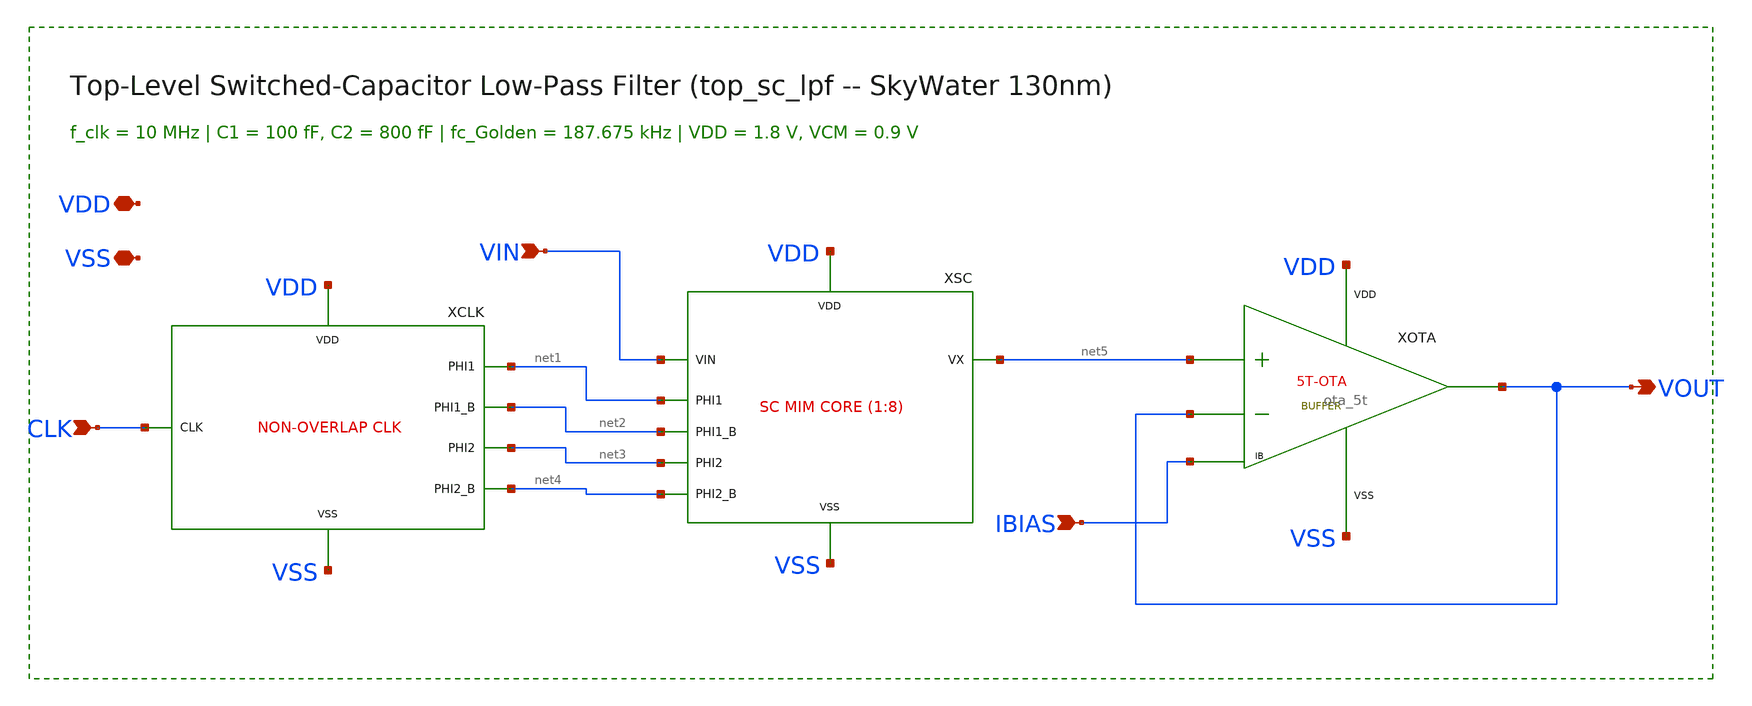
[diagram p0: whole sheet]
** sch_path: sky130-sc-lpf/xschem/top_sc_lpf.sch
**.subckt top_sc_lpf VDD VSS CLK VIN IBIAS VOUT
*.iopin VDD
*.iopin VSS
*.ipin CLK
*.ipin VIN
*.ipin IBIAS
*.opin VOUT
XCLK CLK net1 net2 net3 net4 VDD VSS non_overlap_clk
XSC VIN net5 net1 net2 net3 net4 VDD VSS sc_core
XOTA net5 VOUT IBIAS VOUT VDD VSS ota_5t
**.ends

* expanding   symbol:  non_overlap_clk.sym # of pins=7
** sym_path: sky130-sc-lpf/xschem/non_overlap_clk.sym
** sch_path: sky130-sc-lpf/xschem/non_overlap_clk.sch
.subckt non_overlap_clk CLK PHI1 PHI1_B PHI2 PHI2_B VDD VSS
*.iopin VDD
*.iopin VSS
*.ipin CLK
*.opin PHI1
*.opin PHI1_B
*.opin PHI2
*.opin PHI2_B
XINV0 CLK net1 VDD VSS inv_cell WN=1.0 WP=2.5 LCH=0.15
XNAND_A CLK net15 net2 VDD VSS nand2_cell
XNAND_B net14 net1 net3 VDD VSS nand2_cell
XDA1 net2 net4 VDD VSS inv_cell WN=0.6 WP=1.5 LCH=0.95
XDB1 net3 net5 VDD VSS inv_cell WN=0.6 WP=1.5 LCH=0.95
XDA2 net4 net6 VDD VSS inv_cell WN=0.6 WP=1.5 LCH=0.95
XDB2 net5 net7 VDD VSS inv_cell WN=0.6 WP=1.5 LCH=0.95
XDA3 net6 net8 VDD VSS inv_cell WN=0.6 WP=1.5 LCH=0.95
XDB3 net7 net9 VDD VSS inv_cell WN=0.6 WP=1.5 LCH=0.95
XDA4 net8 net10 VDD VSS inv_cell WN=0.6 WP=1.5 LCH=0.95
XDB4 net9 net11 VDD VSS inv_cell WN=0.6 WP=1.5 LCH=0.95
XDA5 net10 net12 VDD VSS inv_cell WN=0.6 WP=1.5 LCH=0.95
XDB5 net11 net13 VDD VSS inv_cell WN=0.6 WP=1.5 LCH=0.95
XDA6 net12 net14 VDD VSS inv_cell WN=0.6 WP=1.5 LCH=0.95
XDB6 net13 net15 VDD VSS inv_cell WN=0.6 WP=1.5 LCH=0.95
XBUF1A net14 PHI1 VDD VSS inv_cell WN=2.0 WP=6.0 LCH=0.15
XBUF1B PHI1 PHI1_B VDD VSS inv_cell WN=2.0 WP=6.0 LCH=0.15
XBUF2A net15 PHI2 VDD VSS inv_cell WN=2.0 WP=6.0 LCH=0.15
XBUF2B PHI2 PHI2_B VDD VSS inv_cell WN=2.0 WP=6.0 LCH=0.15
.ends


* expanding   symbol:  sc_core.sym # of pins=8
** sym_path: sky130-sc-lpf/xschem/sc_core.sym
** sch_path: sky130-sc-lpf/xschem/sc_core.sch
.subckt sc_core VIN VX PHI1 PHI1_B PHI2 PHI2_B VDD VSS
*.iopin VDD
*.iopin VSS
*.ipin PHI1
*.ipin PHI1_B
*.ipin PHI2
*.ipin PHI2_B
*.ipin VIN
*.opin VX
XTG1 VIN net1 PHI1 PHI1_B VDD VSS tg_switch
XC1 net1 VSS sky130_fd_pr__cap_mim_m3_1 W=4.85 L=9.85 MF=1 m=1
XTG2 net1 VX PHI2 PHI2_B VDD VSS tg_switch
XC2 VX VSS sky130_fd_pr__cap_mim_m3_1 W=4.85 L=9.85 MF=8 m=8
XDUM2 VX PHI2_B PHI2 VDD VSS tg_dummy
.ends


* expanding   symbol:  ota_5t.sym # of pins=6
** sym_path: sky130-sc-lpf/xschem/ota_5t.sym
** sch_path: sky130-sc-lpf/xschem/ota_5t.sch
.subckt ota_5t INP INN IBIAS VOUT VDD VSS
*.iopin VDD
*.opin VOUT
*.ipin INP
*.ipin INN
*.ipin IBIAS
*.iopin VSS
XM3 net1 net1 VDD VDD sky130_fd_pr__pfet_01v8 L=0.80 W=16.0 nf=4 ad='int((nf+1)/2) * W/nf * 0.29' as='int((nf+2)/2) * W/nf * 0.29'
+ pd='2*int((nf+1)/2) * (W/nf + 0.29)' ps='2*int((nf+2)/2) * (W/nf + 0.29)' nrd='0.29 / W' nrs='0.29 / W'
+ sa=0 sb=0 sd=0 mult=1 m=1
XM4 VOUT net1 VDD VDD sky130_fd_pr__pfet_01v8 L=0.80 W=16.0 nf=4 ad='int((nf+1)/2) * W/nf * 0.29' as='int((nf+2)/2) * W/nf * 0.29'
+ pd='2*int((nf+1)/2) * (W/nf + 0.29)' ps='2*int((nf+2)/2) * (W/nf + 0.29)' nrd='0.29 / W' nrs='0.29 / W'
+ sa=0 sb=0 sd=0 mult=1 m=1
XM1 net1 INP net2 VSS sky130_fd_pr__nfet_01v8 L=0.80 W=32.0 nf=8 ad='int((8 + 1)/2) * 32.0 / 8 * 0.29'
+ as='int((8 + 2)/2) * 32.0 / 8 * 0.29' pd='2*int((8 + 1)/2) * (32.0 / 8 + 0.29)' ps='2*int((8 + 2)/2) * (32.0 / 8 + 0.29)'
+ nrd='0.29 / 32.0 ' nrs='0.29 / 32.0 ' sa=0 sb=0 sd=0 mult=1 m=1
XM2 VOUT INN net2 VSS sky130_fd_pr__nfet_01v8 L=0.80 W=32.0 nf=8 ad='int((8 + 1)/2) * 32.0 / 8 * 0.29'
+ as='int((8 + 2)/2) * 32.0 / 8 * 0.29' pd='2*int((8 + 1)/2) * (32.0 / 8 + 0.29)' ps='2*int((8 + 2)/2) * (32.0 / 8 + 0.29)'
+ nrd='0.29 / 32.0 ' nrs='0.29 / 32.0 ' sa=0 sb=0 sd=0 mult=1 m=1
XM5 net2 IBIAS VSS VSS sky130_fd_pr__nfet_01v8 L=1.00 W=24.0 nf=6 ad='int((6 + 1)/2) * 24.0 / 6 * 0.29'
+ as='int((6 + 2)/2) * 24.0 / 6 * 0.29' pd='2*int((6 + 1)/2) * (24.0 / 6 + 0.29)' ps='2*int((6 + 2)/2) * (24.0 / 6 + 0.29)'
+ nrd='0.29 / 24.0 ' nrs='0.29 / 24.0 ' sa=0 sb=0 sd=0 mult=1 m=1
XM6 IBIAS IBIAS VSS VSS sky130_fd_pr__nfet_01v8 L=1.00 W=24.0 nf=6 ad='int((6 + 1)/2) * 24.0 / 6 * 0.29'
+ as='int((6 + 2)/2) * 24.0 / 6 * 0.29' pd='2*int((6 + 1)/2) * (24.0 / 6 + 0.29)' ps='2*int((6 + 2)/2) * (24.0 / 6 + 0.29)'
+ nrd='0.29 / 24.0 ' nrs='0.29 / 24.0 ' sa=0 sb=0 sd=0 mult=1 m=1
.ends


* expanding   symbol:  inv_cell.sym # of pins=4
** sym_path: sky130-sc-lpf/xschem/inv_cell.sym
** sch_path: sky130-sc-lpf/xschem/inv_cell.sch
.subckt inv_cell A Y VDD VSS  WN=1.0 WP=2.5 LCH=0.15
*.ipin A
*.opin Y
*.iopin VDD
*.iopin VSS
XMP Y A VDD VDD sky130_fd_pr__pfet_01v8 L='LCH' W='WP' nf=1 ad='WP*0.29' as='WP*0.29' pd='2*(WP+0.29)'
+ ps='2*(WP+0.29)' nrd='0.29/WP' nrs='0.29/WP' sa=0 sb=0 sd=0 mult=1 m=1
XMN Y A VSS VSS sky130_fd_pr__nfet_01v8 L='LCH' W='WN' nf=1 ad='WN*0.29' as='WN*0.29' pd='2*(WN+0.29)'
+ ps='2*(WN+0.29)' nrd='0.29/WN' nrs='0.29/WN' sa=0 sb=0 sd=0 mult=1 m=1
.ends


* expanding   symbol:  nand2_cell.sym # of pins=5
** sym_path: sky130-sc-lpf/xschem/nand2_cell.sym
** sch_path: sky130-sc-lpf/xschem/nand2_cell.sch
.subckt nand2_cell A B Y VDD VSS
*.iopin VDD
*.opin Y
*.iopin VSS
*.ipin A
*.ipin B
XMPA Y A VDD VDD sky130_fd_pr__pfet_01v8 L=0.15 W=2.0 nf=1 ad='int((nf+1)/2) * W/nf * 0.29' as='int((nf+2)/2) * W/nf * 0.29'
+ pd='2*int((nf+1)/2) * (W/nf + 0.29)' ps='2*int((nf+2)/2) * (W/nf + 0.29)' nrd='0.29 / W' nrs='0.29 / W'
+ sa=0 sb=0 sd=0 mult=1 m=1
XMPB Y B VDD VDD sky130_fd_pr__pfet_01v8 L=0.15 W=2.0 nf=1 ad='int((nf+1)/2) * W/nf * 0.29' as='int((nf+2)/2) * W/nf * 0.29'
+ pd='2*int((nf+1)/2) * (W/nf + 0.29)' ps='2*int((nf+2)/2) * (W/nf + 0.29)' nrd='0.29 / W' nrs='0.29 / W'
+ sa=0 sb=0 sd=0 mult=1 m=1
XMNA Y A net1 VSS sky130_fd_pr__nfet_01v8 L=0.15 W=1.6 nf=1 ad='int((1 + 1)/2) * 1.6 / 1 * 0.29' as='int((1 + 2)/2) * 1.6 / 1 * 0.29'
+ pd='2*int((1 + 1)/2) * (1.6 / 1 + 0.29)' ps='2*int((1 + 2)/2) * (1.6 / 1 + 0.29)' nrd='0.29 / 1.6 ' nrs='0.29 / 1.6 '
+ sa=0 sb=0 sd=0 mult=1 m=1
XMNB net1 B VSS VSS sky130_fd_pr__nfet_01v8 L=0.15 W=1.6 nf=1 ad='int((1 + 1)/2) * 1.6 / 1 * 0.29' as='int((1 + 2)/2) * 1.6 / 1 * 0.29'
+ pd='2*int((1 + 1)/2) * (1.6 / 1 + 0.29)' ps='2*int((1 + 2)/2) * (1.6 / 1 + 0.29)' nrd='0.29 / 1.6 ' nrs='0.29 / 1.6 '
+ sa=0 sb=0 sd=0 mult=1 m=1
.ends


* expanding   symbol:  tg_switch.sym # of pins=6
** sym_path: sky130-sc-lpf/xschem/tg_switch.sym
** sch_path: sky130-sc-lpf/xschem/tg_switch.sch
.subckt tg_switch VIN VOUT PHI PHI_B VDD VSS
*.iopin VIN
*.iopin VOUT
*.ipin PHI_B
*.ipin PHI
*.iopin VDD
*.iopin VSS
XMP VOUT PHI_B VIN VDD sky130_fd_pr__pfet_01v8 L=0.15 W=6.0 nf=2 ad='int((nf+1)/2) * W/nf * 0.29' as='int((nf+2)/2) * W/nf * 0.29'
+ pd='2*int((nf+1)/2) * (W/nf + 0.29)' ps='2*int((nf+2)/2) * (W/nf + 0.29)' nrd='0.29 / W' nrs='0.29 / W'
+ sa=0 sb=0 sd=0 mult=1 m=1
XMN VOUT PHI VIN VSS sky130_fd_pr__nfet_01v8 L=0.15 W=2.0 nf=1 ad='int((1 + 1)/2) * 2.0 / 1 * 0.29' as='int((1 + 2)/2) * 2.0 / 1 * 0.29'
+ pd='2*int((1 + 1)/2) * (2.0 / 1 + 0.29)' ps='2*int((1 + 2)/2) * (2.0 / 1 + 0.29)' nrd='0.29 / 2.0 ' nrs='0.29 / 2.0 '
+ sa=0 sb=0 sd=0 mult=1 m=1
.ends


* expanding   symbol:  tg_dummy.sym # of pins=5
** sym_path: sky130-sc-lpf/xschem/tg_dummy.sym
** sch_path: sky130-sc-lpf/xschem/tg_dummy.sch
.subckt tg_dummy VNODE G_N G_P VDD VSS
*.iopin VNODE
*.ipin G_P
*.ipin G_N
*.iopin VDD
*.iopin VSS
XMPD VNODE G_P VNODE VDD sky130_fd_pr__pfet_01v8 L=0.15 W=3.0 nf=1 ad='int((nf+1)/2) * W/nf * 0.29' as='int((nf+2)/2) * W/nf * 0.29'
+ pd='2*int((nf+1)/2) * (W/nf + 0.29)' ps='2*int((nf+2)/2) * (W/nf + 0.29)' nrd='0.29 / W' nrs='0.29 / W'
+ sa=0 sb=0 sd=0 mult=1 m=1
XMND VNODE G_N VNODE VSS sky130_fd_pr__nfet_01v8 L=0.15 W=1.0 nf=1 ad='int((1 + 1)/2) * 1.0 / 1 * 0.29'
+ as='int((1 + 2)/2) * 1.0 / 1 * 0.29' pd='2*int((1 + 1)/2) * (1.0 / 1 + 0.29)' ps='2*int((1 + 2)/2) * (1.0 / 1 + 0.29)'
+ nrd='0.29 / 1.0 ' nrs='0.29 / 1.0 ' sa=0 sb=0 sd=0 mult=1 m=1
.ends

.end
